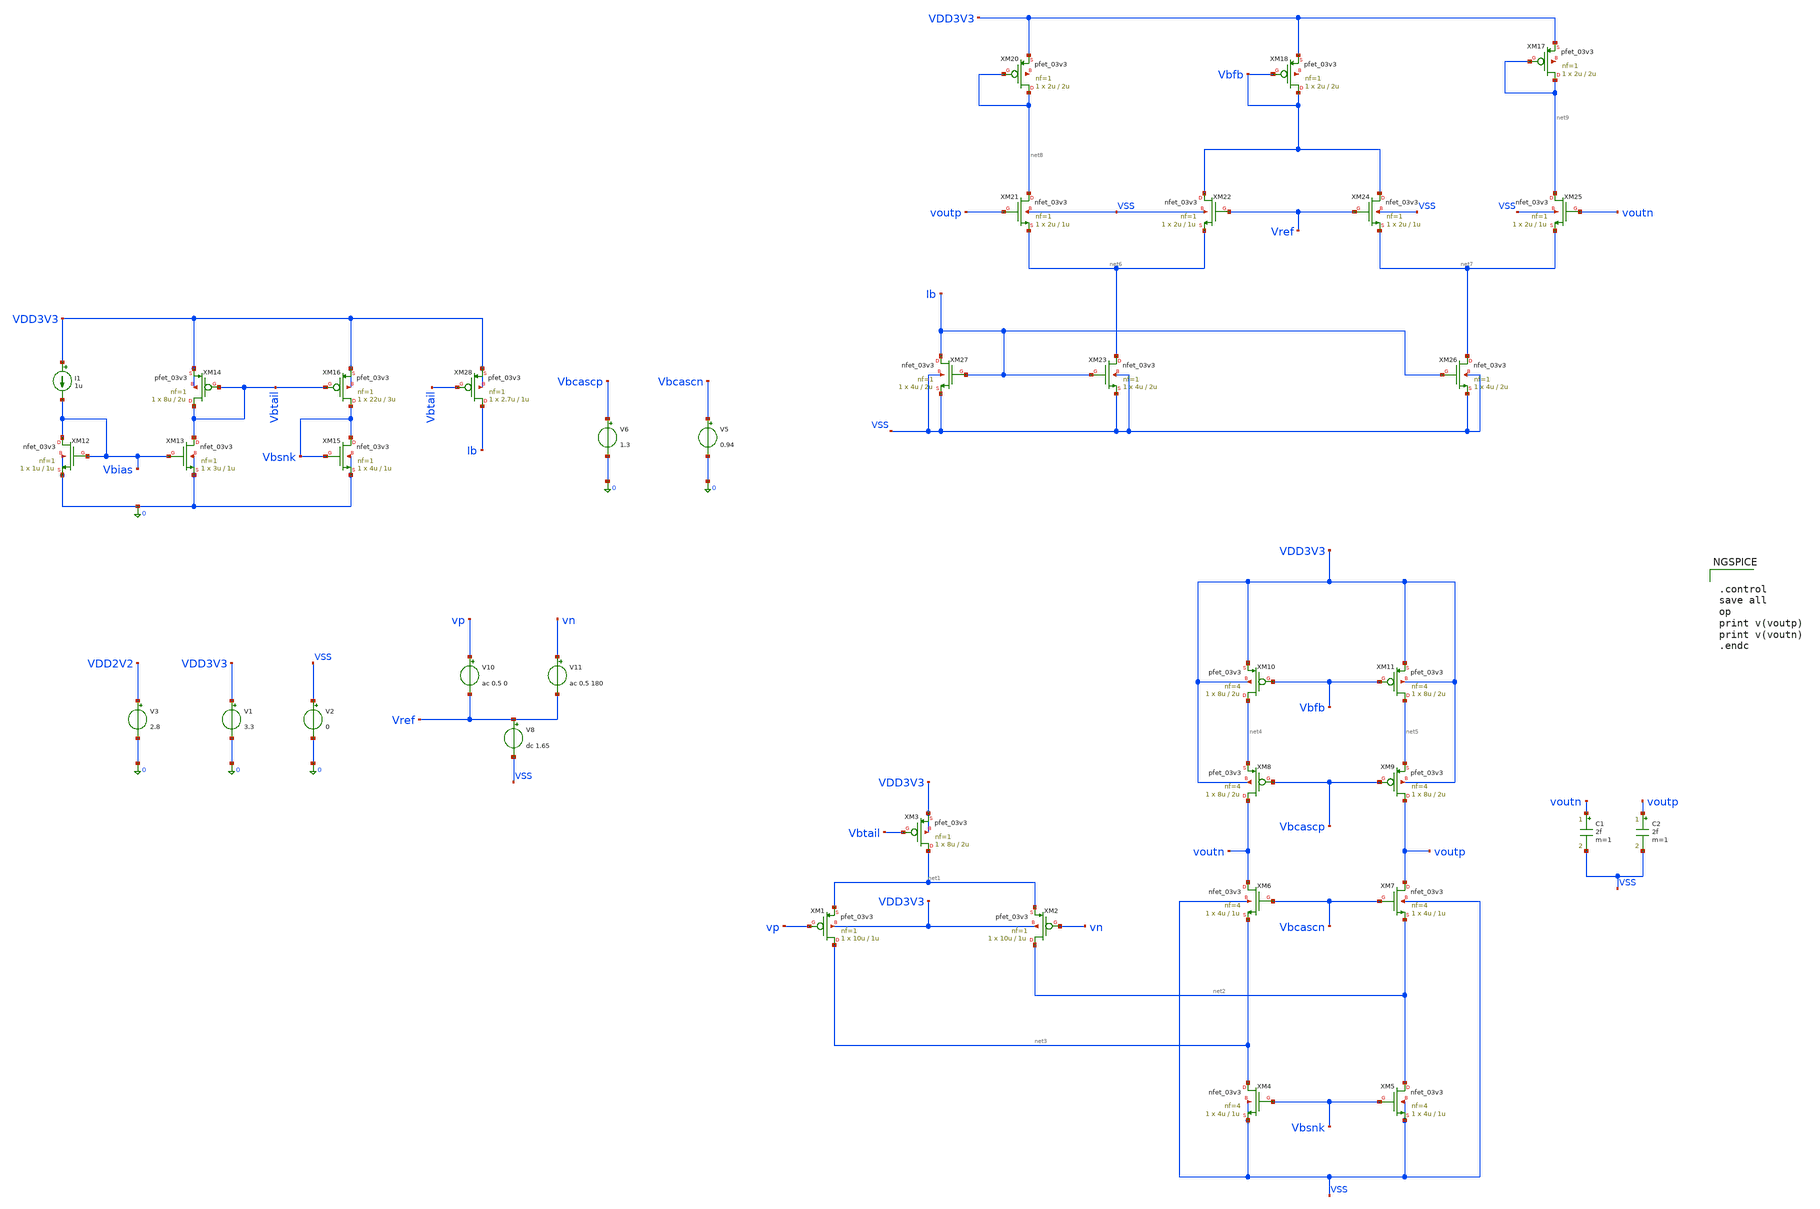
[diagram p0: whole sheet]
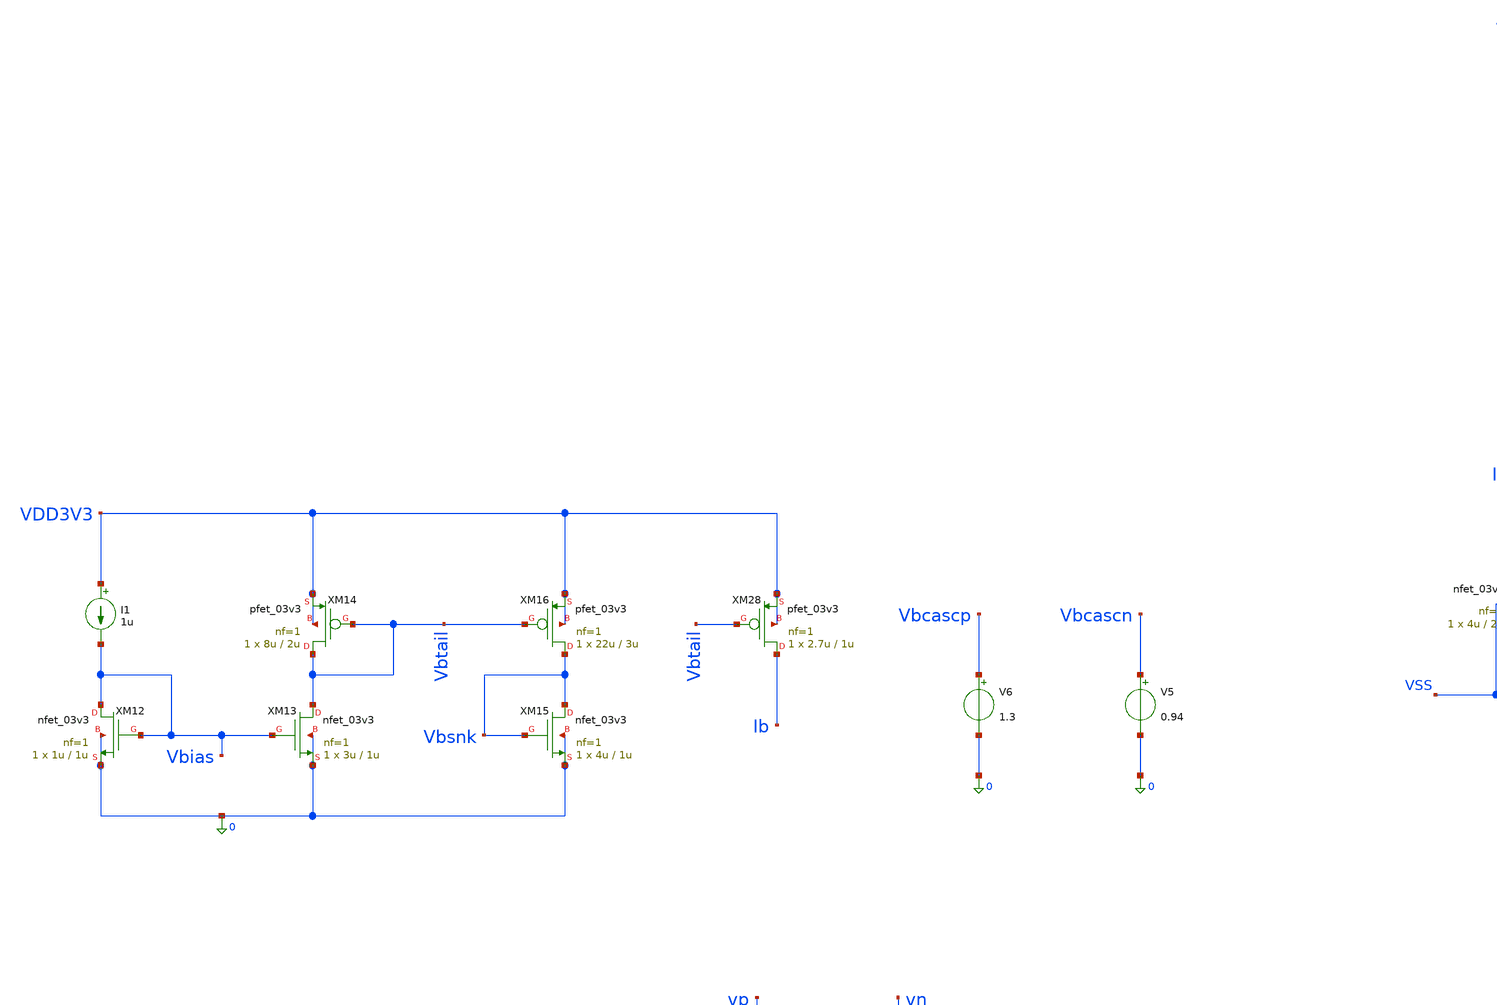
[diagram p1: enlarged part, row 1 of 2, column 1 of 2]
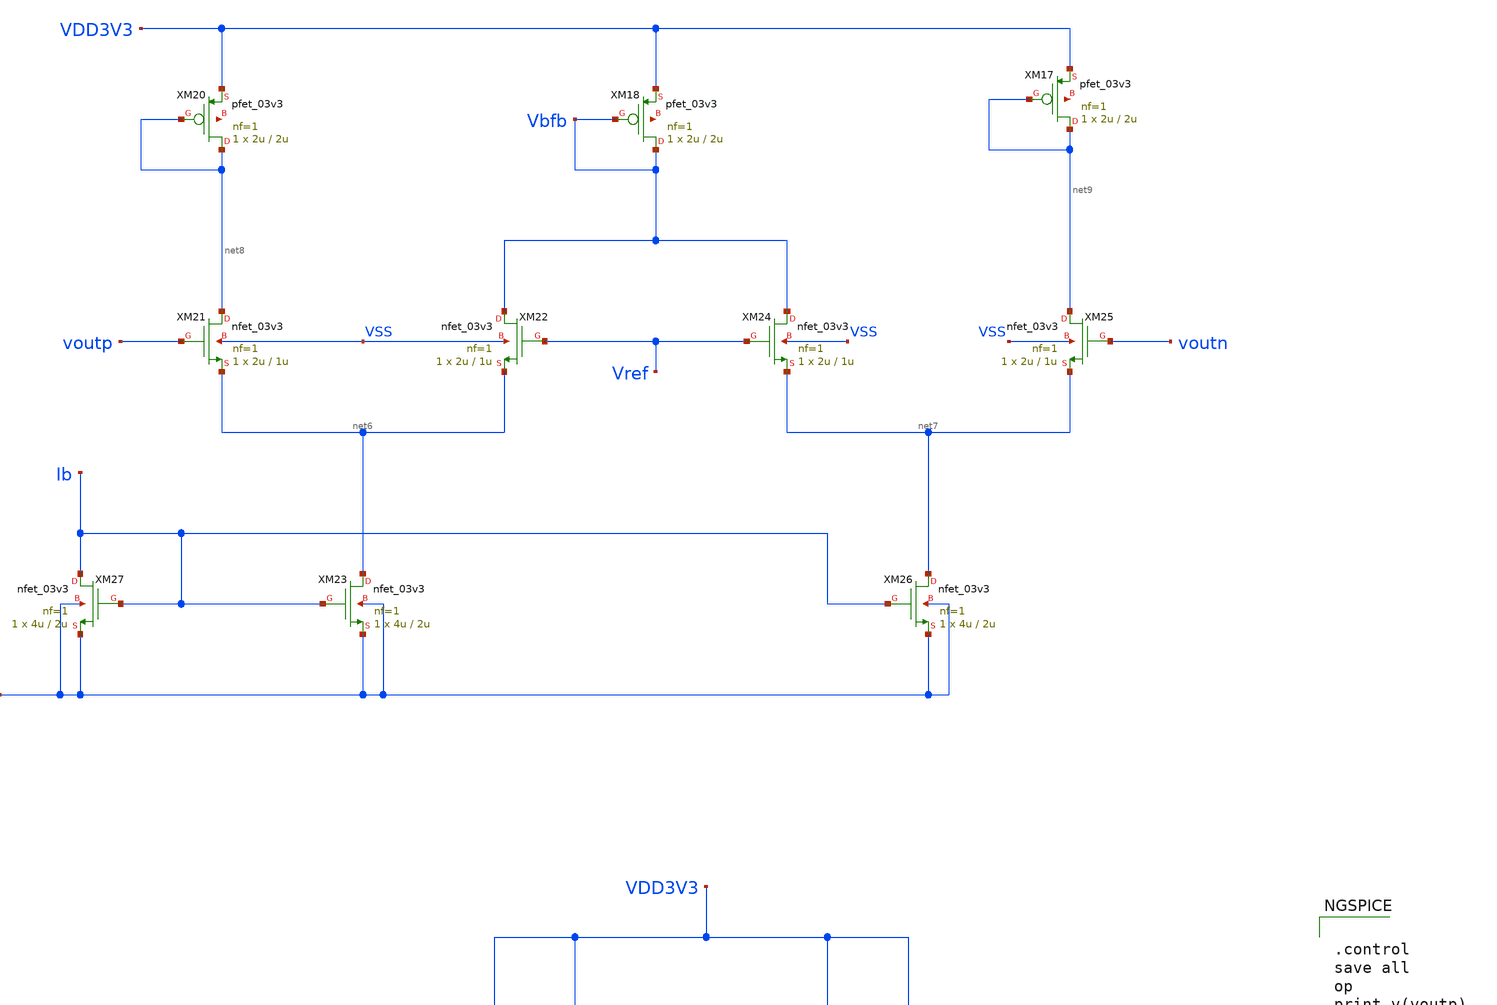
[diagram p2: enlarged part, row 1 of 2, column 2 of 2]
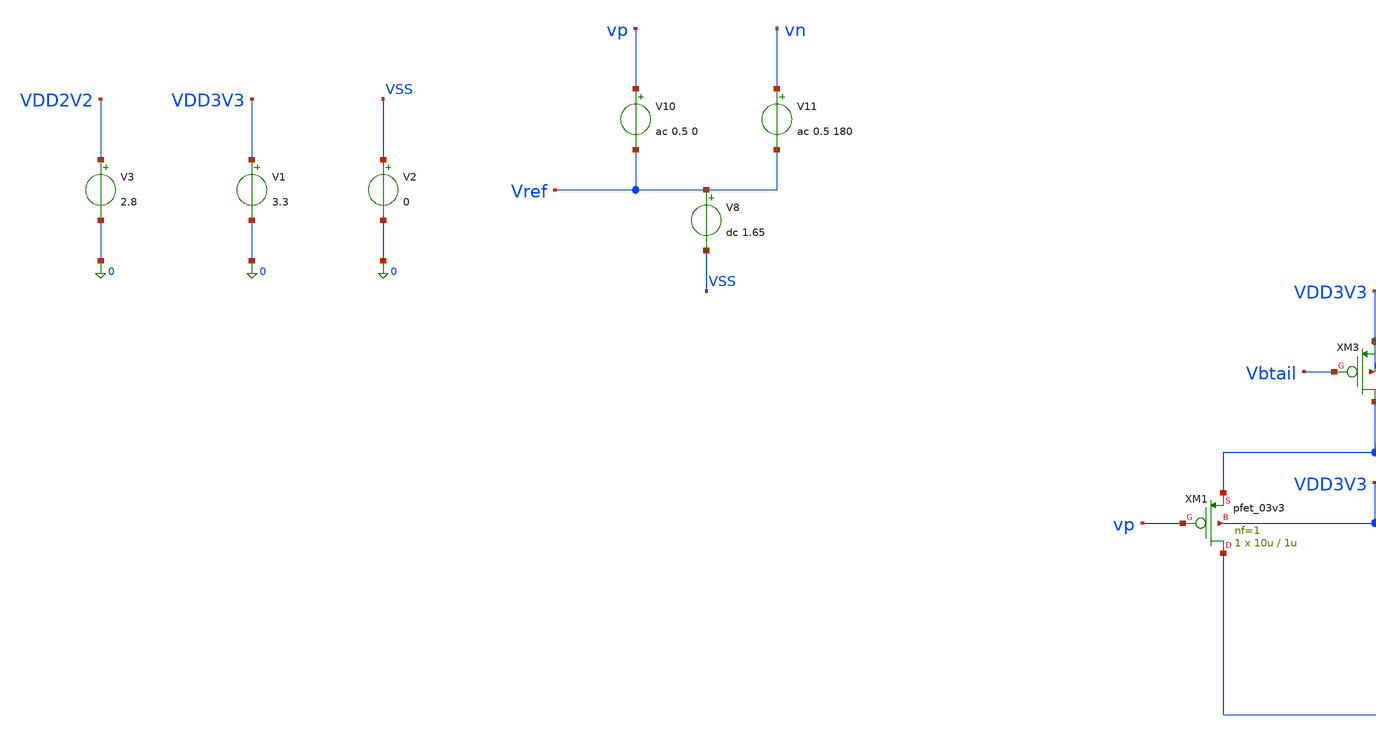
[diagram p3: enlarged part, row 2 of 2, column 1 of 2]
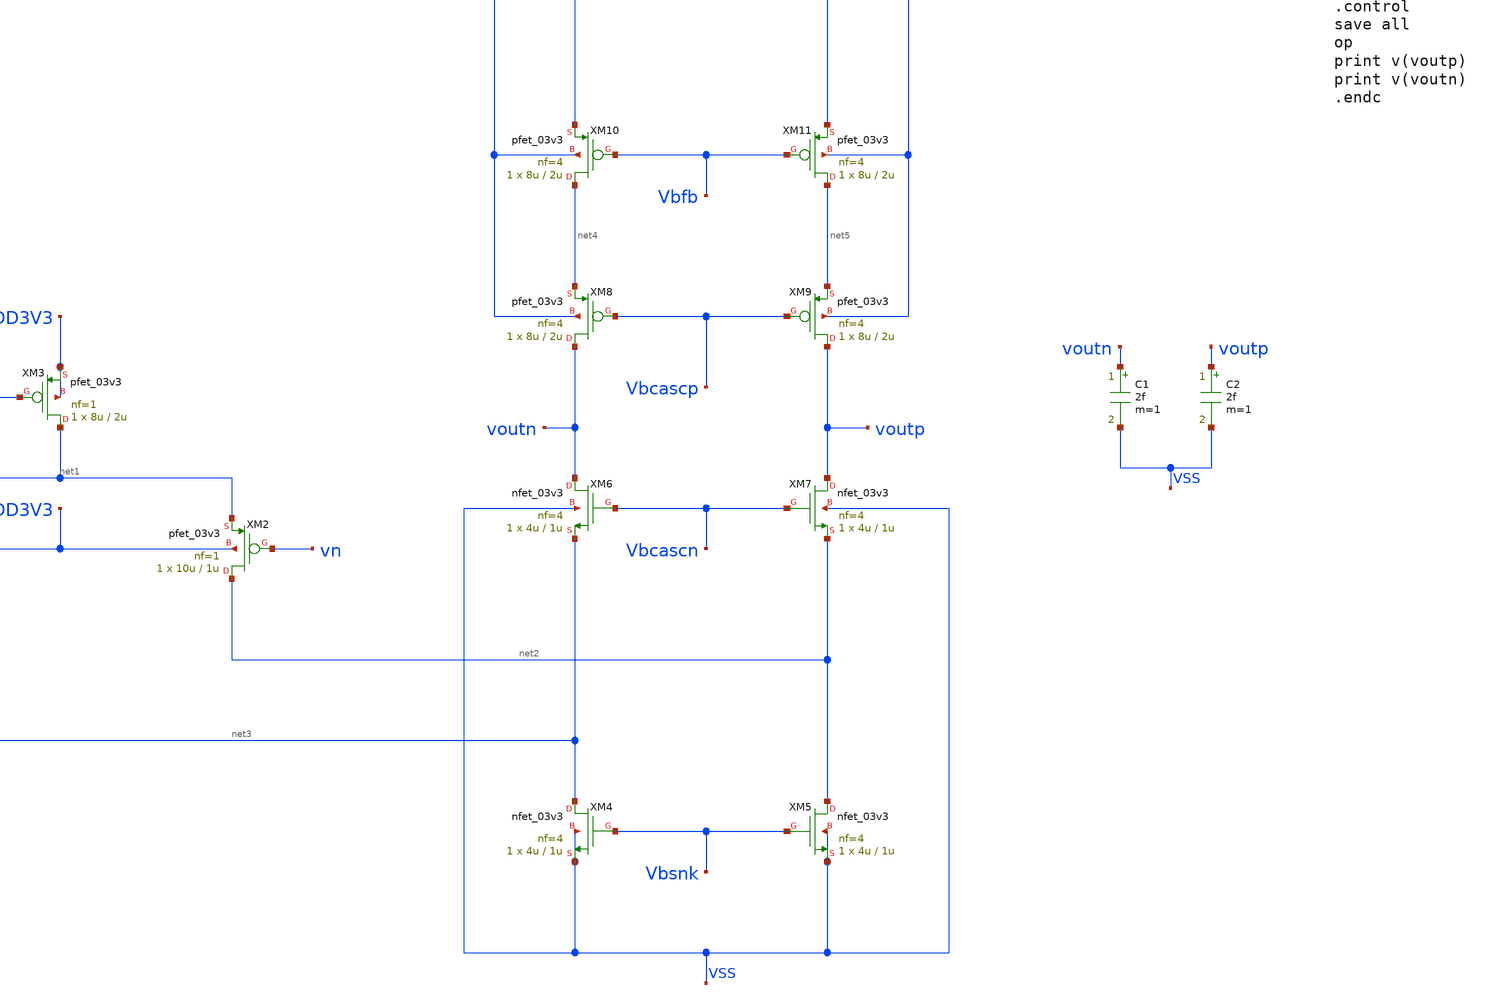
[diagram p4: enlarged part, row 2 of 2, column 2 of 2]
** sch_path: designs/libs/core_pga/folded_cascode/tb_folded_cascode_v3.sch
**.subckt tb_folded_cascode_v3
XM1 net3 vp net1 VDD3V3 pfet_03v3 L=1u W=10u nf=1 ad='int((nf+1)/2) * W/nf * 0.18u' as='int((nf+2)/2) * W/nf * 0.18u'
+ pd='2*int((nf+1)/2) * (W/nf + 0.18u)' ps='2*int((nf+2)/2) * (W/nf + 0.18u)' nrd='0.18u / W' nrs='0.18u / W'
+ sa=0 sb=0 sd=0 m=1
V1 VDD3V3 0 3.3
XM2 net2 vn net1 VDD3V3 pfet_03v3 L=1u W=10u nf=1 ad='int((nf+1)/2) * W/nf * 0.18u' as='int((nf+2)/2) * W/nf * 0.18u'
+ pd='2*int((nf+1)/2) * (W/nf + 0.18u)' ps='2*int((nf+2)/2) * (W/nf + 0.18u)' nrd='0.18u / W' nrs='0.18u / W'
+ sa=0 sb=0 sd=0 m=1
V3 VDD2V2 0 2.8
V5 Vbcascn 0 0.94
V6 Vbcascp 0 1.3
V8 Vref VSS dc 1.65
V10 vp Vref ac 0.5 0
V11 vn Vref ac 0.5 180
XM6 voutn Vbcascn net3 VSS nfet_03v3 L=1u W=4u nf=4 ad='int((nf+1)/2) * W/nf * 0.18u' as='int((nf+2)/2) * W/nf * 0.18u'
+ pd='2*int((nf+1)/2) * (W/nf + 0.18u)' ps='2*int((nf+2)/2) * (W/nf + 0.18u)' nrd='0.18u / W' nrs='0.18u / W'
+ sa=0 sb=0 sd=0 m=1
XM7 voutp Vbcascn net2 VSS nfet_03v3 L=1u W=4u nf=4 ad='int((nf+1)/2) * W/nf * 0.18u' as='int((nf+2)/2) * W/nf * 0.18u'
+ pd='2*int((nf+1)/2) * (W/nf + 0.18u)' ps='2*int((nf+2)/2) * (W/nf + 0.18u)' nrd='0.18u / W' nrs='0.18u / W'
+ sa=0 sb=0 sd=0 m=1
XM8 voutn Vbcascp net4 VDD3V3 pfet_03v3 L=2u W=8u nf=4 ad='int((nf+1)/2) * W/nf * 0.18u' as='int((nf+2)/2) * W/nf * 0.18u'
+ pd='2*int((nf+1)/2) * (W/nf + 0.18u)' ps='2*int((nf+2)/2) * (W/nf + 0.18u)' nrd='0.18u / W' nrs='0.18u / W'
+ sa=0 sb=0 sd=0 m=1
XM9 voutp Vbcascp net5 VDD3V3 pfet_03v3 L=2u W=8u nf=4 ad='int((nf+1)/2) * W/nf * 0.18u' as='int((nf+2)/2) * W/nf * 0.18u'
+ pd='2*int((nf+1)/2) * (W/nf + 0.18u)' ps='2*int((nf+2)/2) * (W/nf + 0.18u)' nrd='0.18u / W' nrs='0.18u / W'
+ sa=0 sb=0 sd=0 m=1
XM3 net1 Vbtail VDD3V3 VDD3V3 pfet_03v3 L=2u W=8u nf=1 ad='int((nf+1)/2) * W/nf * 0.18u' as='int((nf+2)/2) * W/nf * 0.18u'
+ pd='2*int((nf+1)/2) * (W/nf + 0.18u)' ps='2*int((nf+2)/2) * (W/nf + 0.18u)' nrd='0.18u / W' nrs='0.18u / W'
+ sa=0 sb=0 sd=0 m=1
XM4 net3 Vbsnk VSS VSS nfet_03v3 L=1u W=4u nf=4 ad='int((nf+1)/2) * W/nf * 0.18u' as='int((nf+2)/2) * W/nf * 0.18u'
+ pd='2*int((nf+1)/2) * (W/nf + 0.18u)' ps='2*int((nf+2)/2) * (W/nf + 0.18u)' nrd='0.18u / W' nrs='0.18u / W'
+ sa=0 sb=0 sd=0 m=1
XM5 net2 Vbsnk VSS VSS nfet_03v3 L=1u W=4u nf=4 ad='int((nf+1)/2) * W/nf * 0.18u' as='int((nf+2)/2) * W/nf * 0.18u'
+ pd='2*int((nf+1)/2) * (W/nf + 0.18u)' ps='2*int((nf+2)/2) * (W/nf + 0.18u)' nrd='0.18u / W' nrs='0.18u / W'
+ sa=0 sb=0 sd=0 m=1
XM10 net4 Vbfb VDD3V3 VDD3V3 pfet_03v3 L=2u W=8u nf=4 ad='int((nf+1)/2) * W/nf * 0.18u' as='int((nf+2)/2) * W/nf * 0.18u'
+ pd='2*int((nf+1)/2) * (W/nf + 0.18u)' ps='2*int((nf+2)/2) * (W/nf + 0.18u)' nrd='0.18u / W' nrs='0.18u / W'
+ sa=0 sb=0 sd=0 m=1
XM11 net5 Vbfb VDD3V3 VDD3V3 pfet_03v3 L=2u W=8u nf=4 ad='int((nf+1)/2) * W/nf * 0.18u' as='int((nf+2)/2) * W/nf * 0.18u'
+ pd='2*int((nf+1)/2) * (W/nf + 0.18u)' ps='2*int((nf+2)/2) * (W/nf + 0.18u)' nrd='0.18u / W' nrs='0.18u / W'
+ sa=0 sb=0 sd=0 m=1
XM20 net8 net8 VDD3V3 net10 pfet_03v3 L=2u W=2u nf=1 ad='int((nf+1)/2) * W/nf * 0.18u' as='int((nf+2)/2) * W/nf * 0.18u'
+ pd='2*int((nf+1)/2) * (W/nf + 0.18u)' ps='2*int((nf+2)/2) * (W/nf + 0.18u)' nrd='0.18u / W' nrs='0.18u / W'
+ sa=0 sb=0 sd=0 m=1
XM21 net8 voutp net6 VSS nfet_03v3 L=1u W=2u nf=1 ad='int((nf+1)/2) * W/nf * 0.18u' as='int((nf+2)/2) * W/nf * 0.18u'
+ pd='2*int((nf+1)/2) * (W/nf + 0.18u)' ps='2*int((nf+2)/2) * (W/nf + 0.18u)' nrd='0.18u / W' nrs='0.18u / W'
+ sa=0 sb=0 sd=0 m=1
XM22 Vbfb Vref net6 VSS nfet_03v3 L=1u W=2u nf=1 ad='int((nf+1)/2) * W/nf * 0.18u' as='int((nf+2)/2) * W/nf * 0.18u'
+ pd='2*int((nf+1)/2) * (W/nf + 0.18u)' ps='2*int((nf+2)/2) * (W/nf + 0.18u)' nrd='0.18u / W' nrs='0.18u / W'
+ sa=0 sb=0 sd=0 m=1
XM23 net6 Ib VSS VSS nfet_03v3 L=2u W=4u nf=1 ad='int((nf+1)/2) * W/nf * 0.18u' as='int((nf+2)/2) * W/nf * 0.18u'
+ pd='2*int((nf+1)/2) * (W/nf + 0.18u)' ps='2*int((nf+2)/2) * (W/nf + 0.18u)' nrd='0.18u / W' nrs='0.18u / W'
+ sa=0 sb=0 sd=0 m=1
XM24 Vbfb Vref net7 VSS nfet_03v3 L=1u W=2u nf=1 ad='int((nf+1)/2) * W/nf * 0.18u' as='int((nf+2)/2) * W/nf * 0.18u'
+ pd='2*int((nf+1)/2) * (W/nf + 0.18u)' ps='2*int((nf+2)/2) * (W/nf + 0.18u)' nrd='0.18u / W' nrs='0.18u / W'
+ sa=0 sb=0 sd=0 m=1
XM25 net9 voutn net7 VSS nfet_03v3 L=1u W=2u nf=1 ad='int((nf+1)/2) * W/nf * 0.18u' as='int((nf+2)/2) * W/nf * 0.18u'
+ pd='2*int((nf+1)/2) * (W/nf + 0.18u)' ps='2*int((nf+2)/2) * (W/nf + 0.18u)' nrd='0.18u / W' nrs='0.18u / W'
+ sa=0 sb=0 sd=0 m=1
XM26 net7 Ib VSS VSS nfet_03v3 L=2u W=4u nf=1 ad='int((nf+1)/2) * W/nf * 0.18u' as='int((nf+2)/2) * W/nf * 0.18u'
+ pd='2*int((nf+1)/2) * (W/nf + 0.18u)' ps='2*int((nf+2)/2) * (W/nf + 0.18u)' nrd='0.18u / W' nrs='0.18u / W'
+ sa=0 sb=0 sd=0 m=1
XM27 Ib Ib VSS VSS nfet_03v3 L=2u W=4u nf=1 ad='int((nf+1)/2) * W/nf * 0.18u' as='int((nf+2)/2) * W/nf * 0.18u'
+ pd='2*int((nf+1)/2) * (W/nf + 0.18u)' ps='2*int((nf+2)/2) * (W/nf + 0.18u)' nrd='0.18u / W' nrs='0.18u / W'
+ sa=0 sb=0 sd=0 m=1
V2 VSS 0 0
I1 VDD3V3 Vbias 1u
XM12 Vbias Vbias 0 0 nfet_03v3 L=1u W=1u nf=1 ad='int((nf+1)/2) * W/nf * 0.18u' as='int((nf+2)/2) * W/nf * 0.18u'
+ pd='2*int((nf+1)/2) * (W/nf + 0.18u)' ps='2*int((nf+2)/2) * (W/nf + 0.18u)' nrd='0.18u / W' nrs='0.18u / W'
+ sa=0 sb=0 sd=0 m=1
XM13 Vbtail Vbias 0 0 nfet_03v3 L=1u W=3u nf=1 ad='int((nf+1)/2) * W/nf * 0.18u' as='int((nf+2)/2) * W/nf * 0.18u'
+ pd='2*int((nf+1)/2) * (W/nf + 0.18u)' ps='2*int((nf+2)/2) * (W/nf + 0.18u)' nrd='0.18u / W' nrs='0.18u / W'
+ sa=0 sb=0 sd=0 m=1
XM14 Vbtail Vbtail VDD3V3 VDD3V3 pfet_03v3 L=2u W=8u nf=1 ad='int((nf+1)/2) * W/nf * 0.18u' as='int((nf+2)/2) * W/nf * 0.18u'
+ pd='2*int((nf+1)/2) * (W/nf + 0.18u)' ps='2*int((nf+2)/2) * (W/nf + 0.18u)' nrd='0.18u / W' nrs='0.18u / W'
+ sa=0 sb=0 sd=0 m=1
XM15 Vbsnk Vbsnk 0 0 nfet_03v3 L=1u W=4u nf=1 ad='int((nf+1)/2) * W/nf * 0.18u' as='int((nf+2)/2) * W/nf * 0.18u'
+ pd='2*int((nf+1)/2) * (W/nf + 0.18u)' ps='2*int((nf+2)/2) * (W/nf + 0.18u)' nrd='0.18u / W' nrs='0.18u / W'
+ sa=0 sb=0 sd=0 m=1
XM16 Vbsnk Vbtail VDD3V3 VDD3V3 pfet_03v3 L=3u W=22u nf=1 ad='int((nf+1)/2) * W/nf * 0.18u' as='int((nf+2)/2) * W/nf * 0.18u'
+ pd='2*int((nf+1)/2) * (W/nf + 0.18u)' ps='2*int((nf+2)/2) * (W/nf + 0.18u)' nrd='0.18u / W' nrs='0.18u / W'
+ sa=0 sb=0 sd=0 m=1
XM17 net9 net9 VDD3V3 net11 pfet_03v3 L=2u W=2u nf=1 ad='int((nf+1)/2) * W/nf * 0.18u' as='int((nf+2)/2) * W/nf * 0.18u'
+ pd='2*int((nf+1)/2) * (W/nf + 0.18u)' ps='2*int((nf+2)/2) * (W/nf + 0.18u)' nrd='0.18u / W' nrs='0.18u / W'
+ sa=0 sb=0 sd=0 m=1
XM18 Vbfb Vbfb VDD3V3 net12 pfet_03v3 L=2u W=2u nf=1 ad='int((nf+1)/2) * W/nf * 0.18u' as='int((nf+2)/2) * W/nf * 0.18u'
+ pd='2*int((nf+1)/2) * (W/nf + 0.18u)' ps='2*int((nf+2)/2) * (W/nf + 0.18u)' nrd='0.18u / W' nrs='0.18u / W'
+ sa=0 sb=0 sd=0 m=1
XM28 Ib Vbtail VDD3V3 VDD3V3 pfet_03v3 L=1u W=2.7u nf=1 ad='int((nf+1)/2) * W/nf * 0.18u' as='int((nf+2)/2) * W/nf * 0.18u'
+ pd='2*int((nf+1)/2) * (W/nf + 0.18u)' ps='2*int((nf+2)/2) * (W/nf + 0.18u)' nrd='0.18u / W' nrs='0.18u / W'
+ sa=0 sb=0 sd=0 m=1
C1 voutn VSS 2f m=1
C2 voutp VSS 2f m=1
**** begin user architecture code

.include $::180MCU_MODELS/design.ngspice
.lib $::180MCU_MODELS/sm141064.ngspice typical
.lib $::180MCU_MODELS/sm141064.ngspice res_typical
.lib $::180MCU_MODELS/sm141064.ngspice moscap_typical
* .lib $::180MCU_MODELS/sm141064.ngspice res_statistical



.control
save all
op
print v(voutp)
print v(voutn)
.endc




.control
  * 1. Corremos la simulación AC hasta 10 GHz
  ac dec 20 1 10g

  * 2. Definición de la salida diferencial y creación del vector en dB
  let vout = v(voutp) - v(voutn)
  let vout_db = db(vout)

  * 3. Cálculo de la ganancia DC y el objetivo de -3 dB
  let dc_gain_db = vout_db[0]
  let target_3db = dc_gain_db - 3.0

  echo ==================================================
  print dc_gain_db
  print target_3db
  echo ==================================================

  * ==================================================
  * EL TRUCO MAESTRO:
  * Convertimos el número a una variable de entorno de texto (string)
  * ==================================================
  set val_3db = $&target_3db

  * 4. Comandos de medición usando la variable de texto y fall=1
  meas ac f_3db when vout_db=$val_3db fall=1
  meas ac gbw_0db when vout_db=0 fall=1

  * ==================================================

  * 5. Graficar la Magnitud en dB
  plot vout_db

  * 6. Phase Margin calculation
  let voutph = (180/(2*PI))*unwrap(ph(vout))
  plot voutph
  meas ac phase_gbw find voutph when vout_db=0 fall=1
  let phase_margin = 180 + phase_gbw
  print phase_gbw
  print phase_margin
.endc


**** end user architecture code
**.ends
.end
